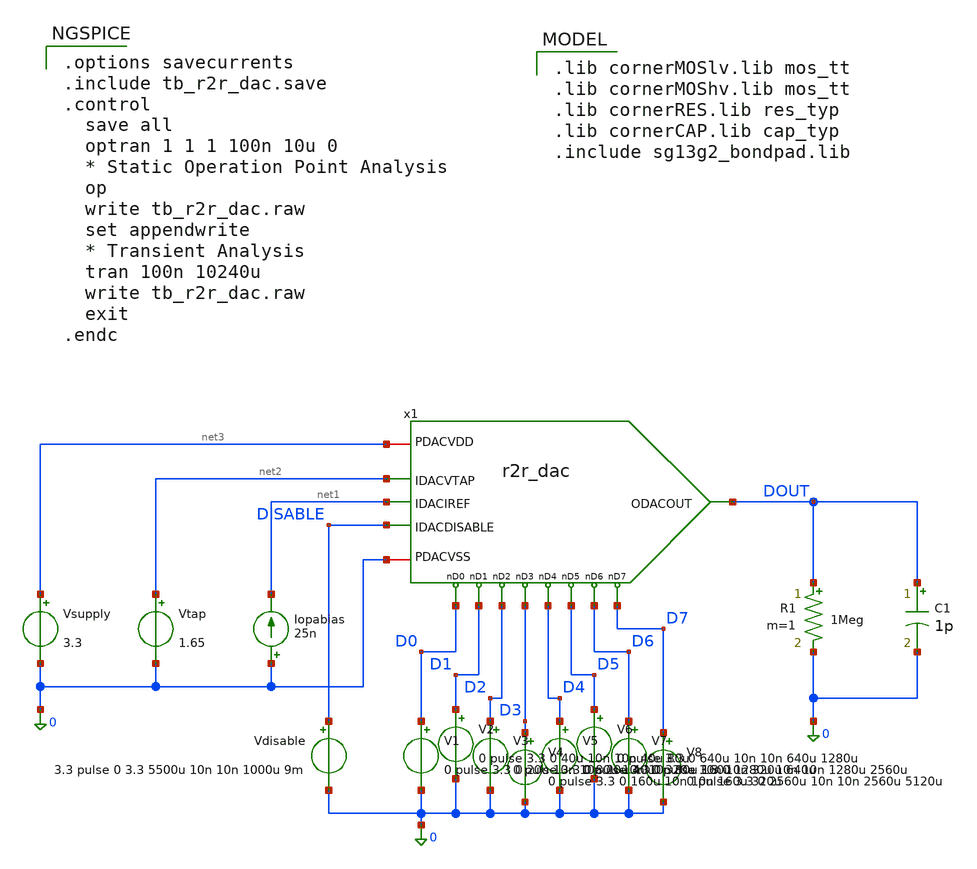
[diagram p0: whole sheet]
** sch_path: macros/heichips26_analog_project/macros/r2r_dac/testbenches/xschem/tb_r2r_dac.sch
**.subckt tb_r2r_dac
x1 net3 DOUT net2 net1 D7 D0 D2 D4 D5 D6 D3 D1 0 DISABLE r2r_dac
Vsupply net3 0 3.3
R1 DOUT 0 1Meg m=1
Vtap net2 0 1.65
Iopabias 0 net1 25n
V1 D0 0 0 pulse 3.3 0 20u 10n 10n 20u 40u
V2 D1 0 0 pulse 3.3 0 40u 10n 10n 40u 80u
V3 D2 0 0 pulse 3.3 0 80u 10n 10n 80u 160u
V4 D3 0 0 pulse 3.3 0 160u 10n 10n 160u 320u
V5 D4 0 0 pulse 3.3 0 320u 10n 10n 320u 640u
V6 D5 0 0 pulse 3.3 0 640u 10n 10n 640u 1280u
V7 D6 0 0 pulse 3.3 0 1280u 10n 10n 1280u 2560u
V8 D7 0 0 pulse 3.3 0 2560u 10n 10n 2560u 5120u
C1 DOUT 0 1p m=1
Vdisable DISABLE 0 3.3 pulse 0 3.3 5500u 10n 10n 1000u 9m
**** begin user architecture code

.options savecurrents
.include tb_r2r_dac.save
.control
  save all
  optran 1 1 1 100n 10u 0
  * Static Operation Point Analysis
  op
  write tb_r2r_dac.raw
  set appendwrite
  * Transient Analysis
  tran 100n 10240u
  write tb_r2r_dac.raw
  exit
.endc



.lib cornerMOSlv.lib mos_tt
.lib cornerMOShv.lib mos_tt
.lib cornerRES.lib res_typ
.lib cornerCAP.lib cap_typ
.include sg13g2_bondpad.lib


**** end user architecture code
**.ends
.end
